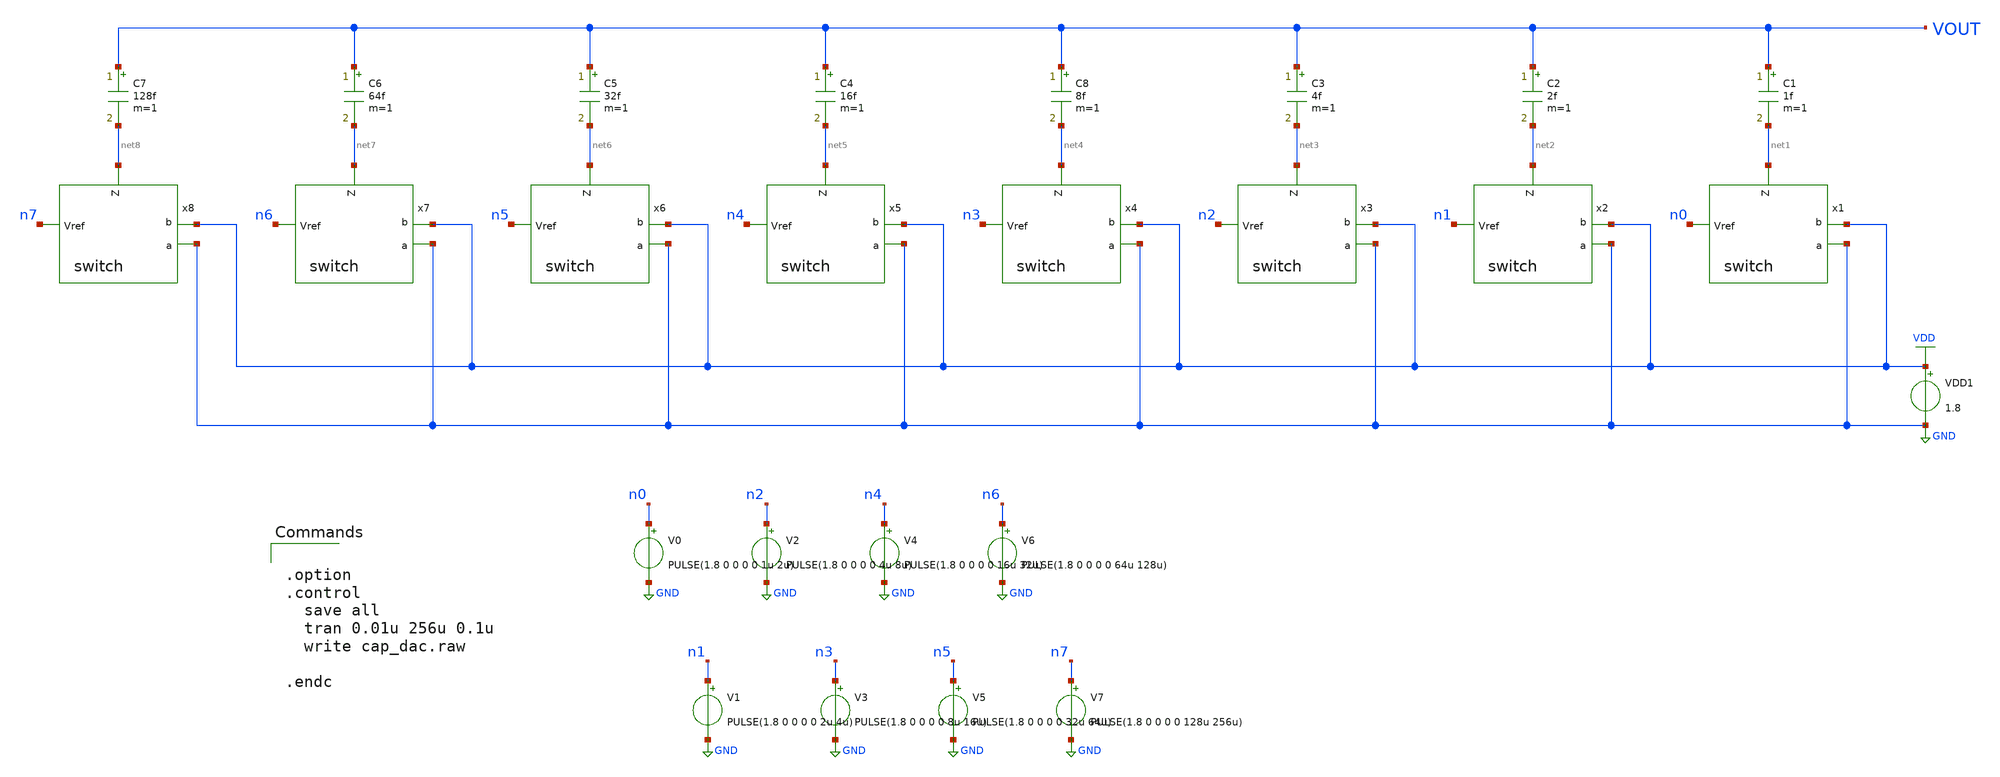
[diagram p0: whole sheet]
** sch_path: cap_dac.sch
**.subckt cap_dac
C1 VOUT net1 1f m=1
VDD1 VDD GND 1.8
C2 VOUT net2 2f m=1
C3 VOUT net3 4f m=1
C8 VOUT net4 8f m=1
C4 VOUT net5 16f m=1
C5 VOUT net6 32f m=1
C6 VOUT net7 64f m=1
C7 VOUT net8 128f m=1
x1 VDD GND net1 n0 switch
x2 VDD GND net2 n1 switch
x3 VDD GND net3 n2 switch
x4 VDD GND net4 n3 switch
x5 VDD GND net5 n4 switch
x6 VDD GND net6 n5 switch
x7 VDD GND net7 n6 switch
x8 VDD GND net8 n7 switch
V1 n1 GND PULSE(1.8 0 0 0 0 2u 4u)
V2 n2 GND PULSE(1.8 0 0 0 0 4u 8u)
V3 n3 GND PULSE(1.8 0 0 0 0 8u 16u)
V4 n4 GND PULSE(1.8 0 0 0 0 16u 32u)
V5 n5 GND PULSE(1.8 0 0 0 0 32u 64u)
V6 n6 GND PULSE(1.8 0 0 0 0 64u 128u)
V7 n7 GND PULSE(1.8 0 0 0 0 128u 256u)
V0 n0 GND PULSE(1.8 0 0 0 0 1u 2u)
**** begin user architecture code

** opencircuitdesign pdks install
.lib $::SKYWATER_MODELS/sky130.lib.spice tt




.option
.control
  save all
  tran 0.01u 256u 0.1u
  write cap_dac.raw

.endc


**** end user architecture code
**.ends

* expanding   symbol:  /foss/designs/MICRO_1_2425_2/switch.sym # of pins=4
** sym_path: switch.sym
** sch_path: switch.sch
.subckt switch b a Z Vref
*.ipin Vref
*.iopin Z
*.iopin a
*.iopin b
XM27 a Vref Z VDD sky130_fd_pr__pfet_01v8 L=0.15 W=1 nf=1 ad='int((1 + 1)/2) * 1 / 1 * 0.29' as='int((1 + 2)/2) * 1 / 1 * 0.29'
+ pd='2*int((1 + 1)/2) * (1 / 1 + 0.29)' ps='2*int((1 + 2)/2) * (1 / 1 + 0.29)' nrd='0.29 / 1 ' nrs='0.29 / 1 '
+ sa=0 sb=0 sd=0 mult=1 m=1
XM18 Z net1 a GND sky130_fd_pr__nfet_01v8 L=0.15 W=1 nf=1 ad='int((nf+1)/2) * W/nf * 0.29' as='int((nf+2)/2) * W/nf * 0.29'
+ pd='2*int((nf+1)/2) * (W/nf + 0.29)' ps='2*int((nf+2)/2) * (W/nf + 0.29)' nrd='0.29 / W' nrs='0.29 / W'
+ sa=0 sb=0 sd=0 mult=1 m=1
XM1 b net1 Z VDD sky130_fd_pr__pfet_01v8 L=0.15 W=1 nf=1 ad='int((1 + 1)/2) * 1 / 1 * 0.29' as='int((1 + 2)/2) * 1 / 1 * 0.29'
+ pd='2*int((1 + 1)/2) * (1 / 1 + 0.29)' ps='2*int((1 + 2)/2) * (1 / 1 + 0.29)' nrd='0.29 / 1 ' nrs='0.29 / 1 '
+ sa=0 sb=0 sd=0 mult=1 m=1
XM2 Z Vref b GND sky130_fd_pr__nfet_01v8 L=0.15 W=1 nf=1 ad='int((nf+1)/2) * W/nf * 0.29' as='int((nf+2)/2) * W/nf * 0.29'
+ pd='2*int((nf+1)/2) * (W/nf + 0.29)' ps='2*int((nf+2)/2) * (W/nf + 0.29)' nrd='0.29 / W' nrs='0.29 / W'
+ sa=0 sb=0 sd=0 mult=1 m=1
XM49 net1 Vref GND GND sky130_fd_pr__nfet_01v8 L=0.15 W=1 nf=1 ad='int((nf+1)/2) * W/nf * 0.29' as='int((nf+2)/2) * W/nf * 0.29'
+ pd='2*int((nf+1)/2) * (W/nf + 0.29)' ps='2*int((nf+2)/2) * (W/nf + 0.29)' nrd='0.29 / W' nrs='0.29 / W'
+ sa=0 sb=0 sd=0 mult=1 m=1
XM50 net1 Vref VDD VDD sky130_fd_pr__pfet_01v8 L=0.15 W=1 nf=1 ad='int((1 + 1)/2) * 1 / 1 * 0.29' as='int((1 + 2)/2) * 1 / 1 * 0.29'
+ pd='2*int((1 + 1)/2) * (1 / 1 + 0.29)' ps='2*int((1 + 2)/2) * (1 / 1 + 0.29)' nrd='0.29 / 1 ' nrs='0.29 / 1 '
+ sa=0 sb=0 sd=0 mult=1 m=1
.ends

.GLOBAL GND
.GLOBAL VDD
.end
